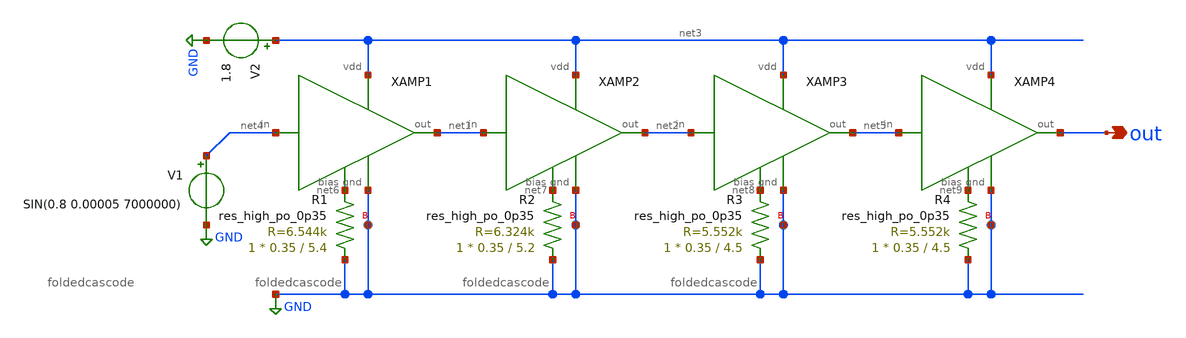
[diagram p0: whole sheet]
** sch_path: xschem/lna/lna4stage.sch
**.subckt lna4stage out
*.opin out
XAMP1 net4 GND net1 net3 net6 foldedcascode
XAMP2 net1 GND net2 net3 net7 foldedcascode
XAMP3 net2 GND net5 net3 net8 foldedcascode
V1 net4 GND SIN(0.8 0.00005 7000000)
V2 net3 GND 1.8
XAMP4 net5 GND out net3 net9 foldedcascode
XR1 GND net6 GND sky130_fd_pr__res_high_po_0p35 L=5.4 mult=1 m=1
XR2 GND net7 GND sky130_fd_pr__res_high_po_0p35 L=5.2 mult=1 m=1
XR3 GND net8 GND sky130_fd_pr__res_high_po_0p35 L=4.5 mult=1 m=1
XR4 GND net9 GND sky130_fd_pr__res_high_po_0p35 L=4.5 mult=1 m=1
**** begin user architecture code


.lib /foss/pdk/sky130A/libs.tech/ngspice/sky130.lib.spice tt
.control
	** dc V1 0.769 3.769 0.01
	** dc V2 0 3 0.01
        ** SIN(0.9 0.00001 700000000)
	tran 0.0000000001 0.000001
	** ac lin 500 1K 100MEG
	** plot vdb(out1) xlog
.endc
.save all


 ** manual skywater pdks install (with patches applied)
* .lib $::SKYWATER_MODELS/models/sky130.lib.spice tt

** opencircuitdesign pdks install
.lib /foss/pdk/sky130A/libs.tech/ngspice/sky130.lib.spice tt

.param mc_mm_switch=0
.param mc_pr_switch=0

**** end user architecture code
**.ends
.GLOBAL GND
.end
